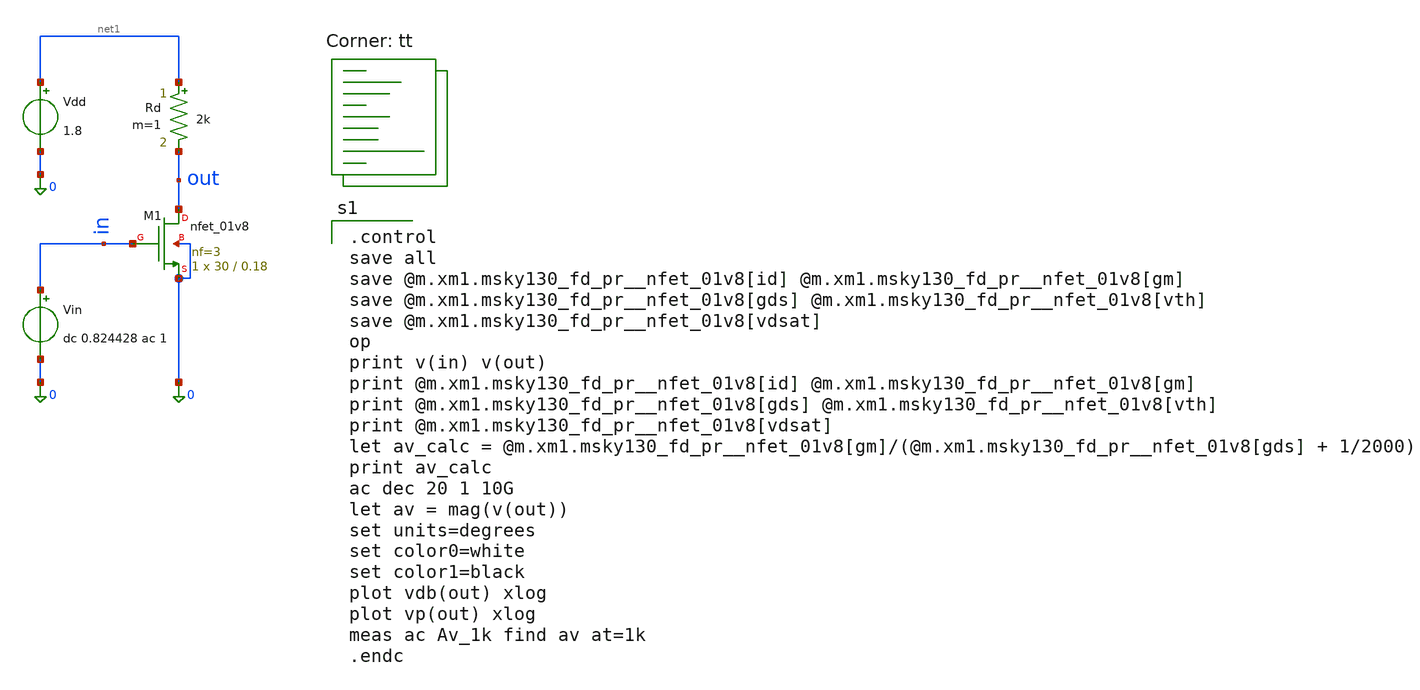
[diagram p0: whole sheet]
** sch_path: Homework 6 - Simulation on Open Source Softwares/Simulations/ex4_final.sch
**.subckt ex4_final
XM1 out in 0 0 sky130_fd_pr__nfet_01v8 L=0.18 W=30 nf=3 ad='int((3 + 1)/2) * 30 / 3 * 0.29' as='int((3 + 2)/2) * 30 / 3 * 0.29'
+ pd='2*int((3 + 1)/2) * (30 / 3 + 0.29)' ps='2*int((3 + 2)/2) * (30 / 3 + 0.29)' nrd='0.29 / 30 ' nrs='0.29 / 30 '
+ sa=0 sb=0 sd=0 mult=1 m=1
Vin in 0 dc 0.824428 ac 1
Rd net1 out 2k m=1
Vdd net1 0 1.8
**** begin user architecture code
.lib $::SKYWATER_MODELS/sky130.lib.spice tt

.control
save all
save @m.xm1.msky130_fd_pr__nfet_01v8[id] @m.xm1.msky130_fd_pr__nfet_01v8[gm]
save @m.xm1.msky130_fd_pr__nfet_01v8[gds] @m.xm1.msky130_fd_pr__nfet_01v8[vth]
save @m.xm1.msky130_fd_pr__nfet_01v8[vdsat]
op
print v(in) v(out)
print @m.xm1.msky130_fd_pr__nfet_01v8[id] @m.xm1.msky130_fd_pr__nfet_01v8[gm]
print @m.xm1.msky130_fd_pr__nfet_01v8[gds] @m.xm1.msky130_fd_pr__nfet_01v8[vth]
print @m.xm1.msky130_fd_pr__nfet_01v8[vdsat]
let av_calc = @m.xm1.msky130_fd_pr__nfet_01v8[gm]/(@m.xm1.msky130_fd_pr__nfet_01v8[gds] + 1/2000)
print av_calc
ac dec 20 1 10G
let av = mag(v(out))
set units=degrees
set color0=white
set color1=black
plot vdb(out) xlog
plot vp(out) xlog
meas ac Av_1k find av at=1k
.endc

**** end user architecture code
**.ends
.end
